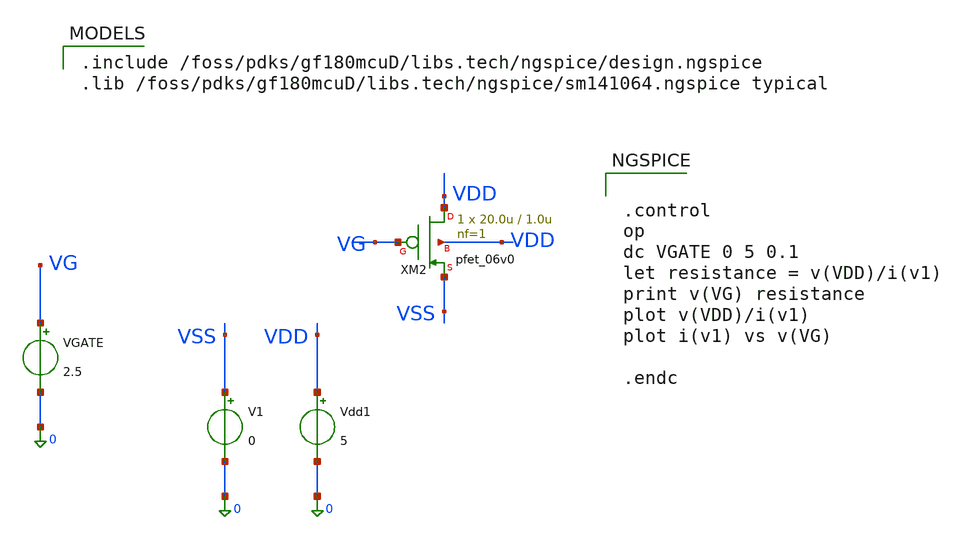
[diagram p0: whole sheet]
** sch_path: activities/opamp3An/pfetVGScheck.sch
**.subckt pfetVGScheck
XM2 VDD VG VSS VDD pfet_06v0 L=1.0u W=20.0u nf=1 ad='int((nf+1)/2) * W/nf * 0.18u' as='int((nf+2)/2) * W/nf * 0.18u'
+ pd='2*int((nf+1)/2) * (W/nf + 0.18u)' ps='2*int((nf+2)/2) * (W/nf + 0.18u)' nrd='0.18u / W' nrs='0.18u / W'
+ sa=0 sb=0 sd=0 m=1
VGATE VG 0 2.5
V1 VSS 0 0
Vdd1 VDD 0 5
**** begin user architecture code

.include /foss/pdks/gf180mcuD/libs.tech/ngspice/design.ngspice
.lib /foss/pdks/gf180mcuD/libs.tech/ngspice/sm141064.ngspice typical



.control
op
dc VGATE 0 5 0.1
let resistance = v(VDD)/i(v1)
print v(VG) resistance
plot v(VDD)/i(v1)
plot i(v1) vs v(VG)

.endc

**** end user architecture code
**.ends
.end
